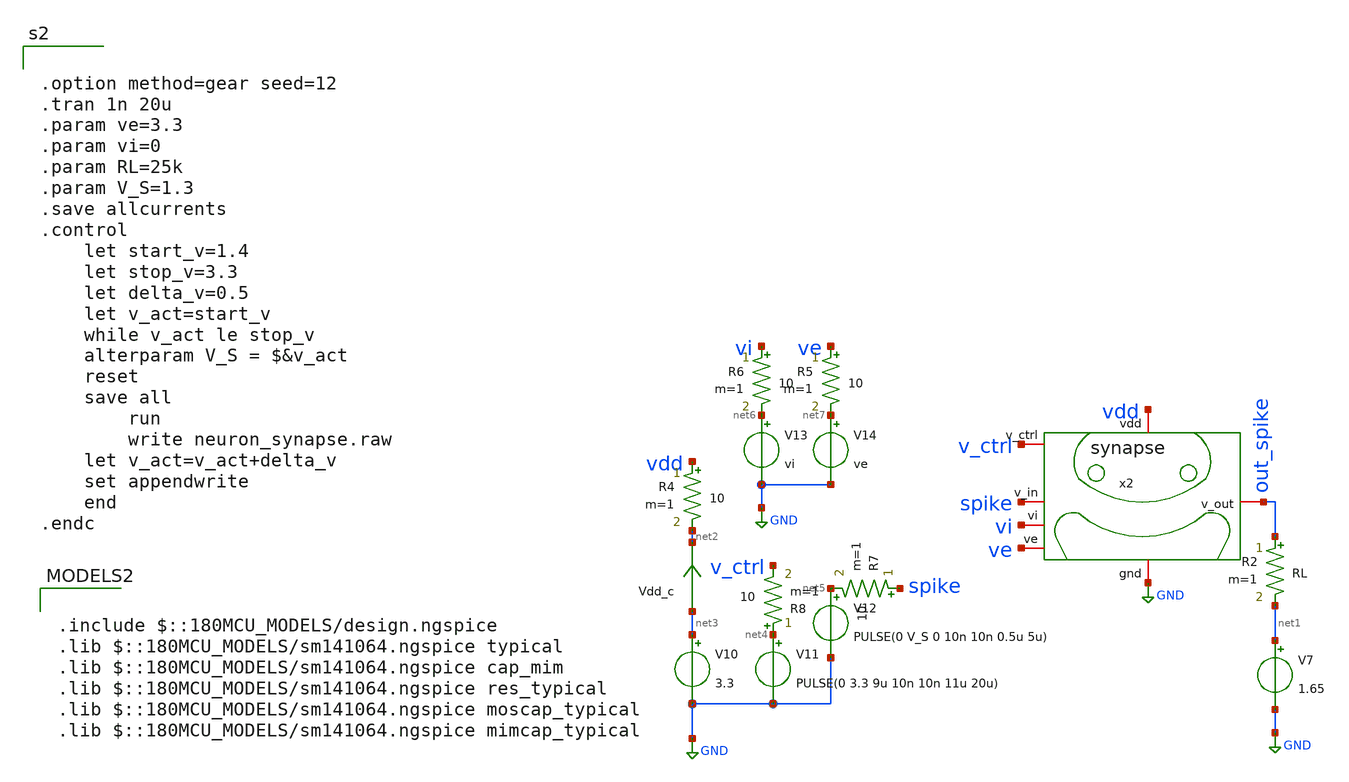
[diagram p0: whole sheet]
** sch_path: designs/libs/tb_neuron_synapse/neuron_synapse.sch
**.subckt neuron_synapse
V7 net1 GND 1.65
R2 out_spike net1 RL m=1
x2 vdd spike ve v_ctrl out_spike vi GND synapse
V10 net3 GND 3.3
Vdd_c net3 net2 0
.save i(vdd_c)
V11 net4 GND PULSE(0 3.3 9u 10n 10n 11u 20u)
V12 net5 GND PULSE(0 V_S 0 10n 10n 0.5u 5u)
V13 net6 GND vi
V14 net7 GND ve
R4 vdd net2 10 m=1
R5 ve net7 10 m=1
R6 vi net6 10 m=1
R7 spike net5 10 m=1
R8 net4 v_ctrl 10 m=1
**** begin user architecture code


.option method=gear seed=12
.tran 1n 20u
.param ve=3.3
.param vi=0
.param RL=25k
.param V_S=1.3
.save allcurrents
.control
    let start_v=1.4
    let stop_v=3.3
    let delta_v=0.5
    let v_act=start_v
    while v_act le stop_v
	alterparam V_S = $&v_act
	reset
	save all
        run
        write neuron_synapse.raw
	let v_act=v_act+delta_v
	set appendwrite
    end
.endc



.include $::180MCU_MODELS/design.ngspice
.lib $::180MCU_MODELS/sm141064.ngspice typical
.lib $::180MCU_MODELS/sm141064.ngspice cap_mim
.lib $::180MCU_MODELS/sm141064.ngspice res_typical
.lib $::180MCU_MODELS/sm141064.ngspice moscap_typical
.lib $::180MCU_MODELS/sm141064.ngspice mimcap_typical

**** end user architecture code
**.ends
.GLOBAL GND
.end
